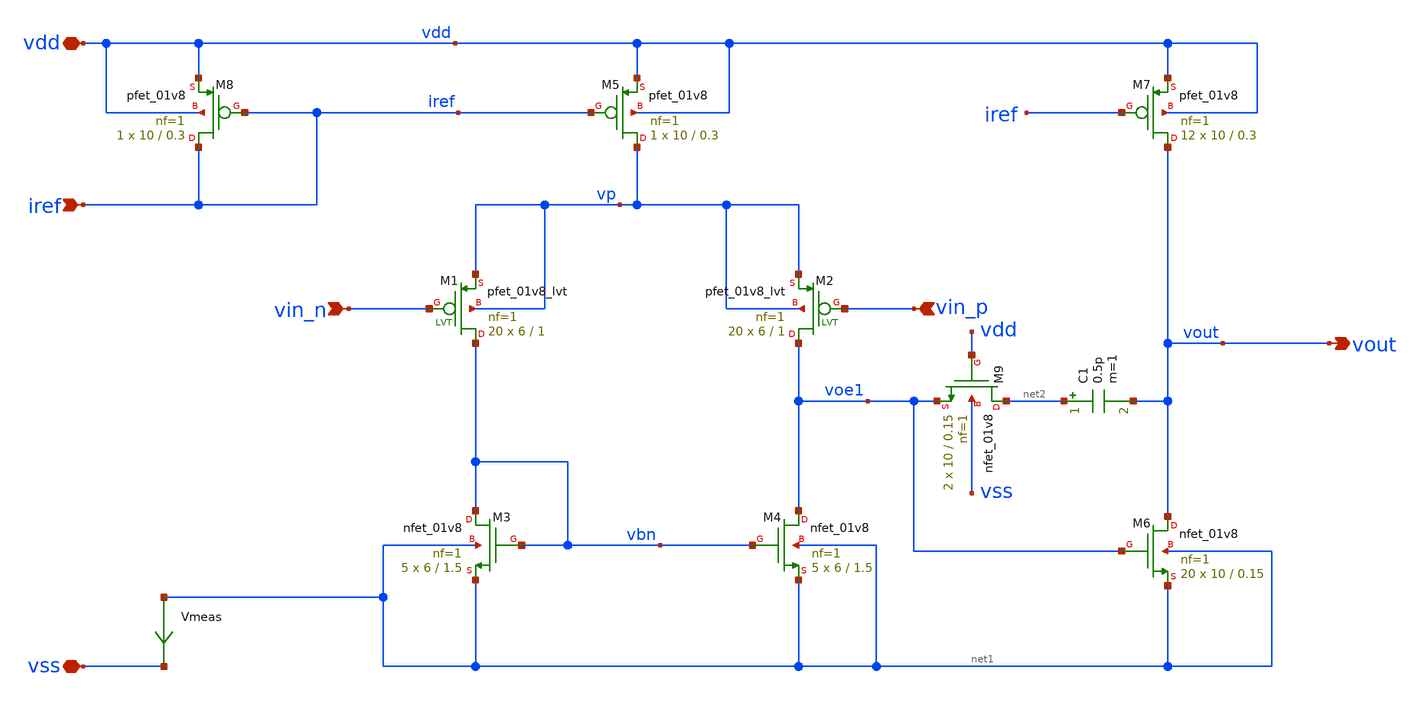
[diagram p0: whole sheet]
** sch_path: opamp/opamp.sch
**.subckt opamp vdd vss vin_n vin_p iref vout
*.iopin vdd
*.iopin vss
*.ipin vin_n
*.ipin vin_p
*.ipin iref
*.opin vout
XM3 vbn vbn net1 net1 sky130_fd_pr__nfet_01v8 L=1.5 W=6 nf=1 ad='W * 0.29' as='W * 0.29' pd='2 * (W + 0.29)'
+ ps='2 * (W + 0.29)' nrd='0.29 / W' nrs='0.29 / W' sa=0 sb=0 sd=0 mult=5 m=5
XM4 voe1 vbn net1 net1 sky130_fd_pr__nfet_01v8 L=1.5 W=6 nf=1 ad='W * 0.29' as='W * 0.29' pd='2 * (W + 0.29)'
+ ps='2 * (W + 0.29)' nrd='0.29 / W' nrs='0.29 / W' sa=0 sb=0 sd=0 mult=5 m=5
XM5 vp iref vdd vdd sky130_fd_pr__pfet_01v8 L=0.3 W=10 nf=1 ad='W * 0.29' as='W * 0.29' pd='2 * (W + 0.29)'
+ ps='2 * (W + 0.29)' nrd='0.29 / W' nrs='0.29 / W' sa=0 sb=0 sd=0 mult=1 m=1
XM7 vout iref vdd vdd sky130_fd_pr__pfet_01v8 L=0.3 W=10 nf=1 ad='W * 0.29' as='W * 0.29' pd='2 * (W + 0.29)'
+ ps='2 * (W + 0.29)' nrd='0.29 / W' nrs='0.29 / W' sa=0 sb=0 sd=0 mult=12 m=12
XM8 iref iref vdd vdd sky130_fd_pr__pfet_01v8 L=0.3 W=10 nf=1 ad='W * 0.29' as='W * 0.29' pd='2 * (W + 0.29)'
+ ps='2 * (W + 0.29)' nrd='0.29 / W' nrs='0.29 / W' sa=0 sb=0 sd=0 mult=1 m=1
XM9 net2 vdd voe1 vss sky130_fd_pr__nfet_01v8 L=0.15 W=10 nf=1 ad='W * 0.29' as='W * 0.29' pd='2 * (W + 0.29)'
+ ps='2 * (W + 0.29)' nrd='0.29 / W' nrs='0.29 / W' sa=0 sb=0 sd=0 mult=2 m=2
XM6 vout voe1 net1 net1 sky130_fd_pr__nfet_01v8 L=0.15 W=10 nf=1 ad='W * 0.29' as='W * 0.29' pd='2 * (W + 0.29)'
+ ps='2 * (W + 0.29)' nrd='0.29 / W' nrs='0.29 / W' sa=0 sb=0 sd=0 mult=20 m=20
XM1 vbn vin_n vp vp sky130_fd_pr__pfet_01v8_lvt L=1 W=6 nf=1 ad='int((nf+1)/2) * W/nf * 0.29' as='int((nf+2)/2) * W/nf * 0.29'
+ pd='2*int((nf+1)/2) * (W/nf + 0.29)' ps='2*int((nf+2)/2) * (W/nf + 0.29)' nrd='0.29 / W' nrs='0.29 / W'
+ sa=0 sb=0 sd=0 mult=20 m=20
XM2 voe1 vin_p vp vp sky130_fd_pr__pfet_01v8_lvt L=1 W=6 nf=1 ad='int((nf+1)/2) * W/nf * 0.29' as='int((nf+2)/2) * W/nf * 0.29'
+ pd='2*int((nf+1)/2) * (W/nf + 0.29)' ps='2*int((nf+2)/2) * (W/nf + 0.29)' nrd='0.29 / W' nrs='0.29 / W'
+ sa=0 sb=0 sd=0 mult=20 m=20
C1 net2 vout 0.5p m=1
Vmeas net1 vss 0
.save i(vmeas)
**.ends
.end
